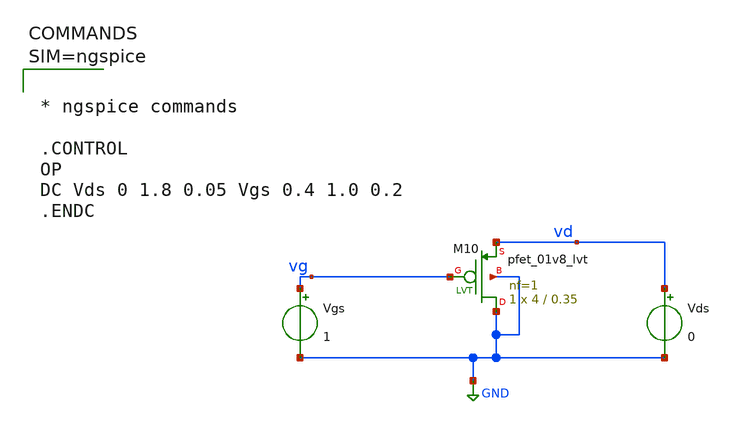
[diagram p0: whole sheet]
** sch_path: work/xschem/nmos_8.sch
**.subckt nmos_8
Vgs vg GND 1
Vds vd GND 0
XM10 GND vg vd GND sky130_fd_pr__pfet_01v8_lvt L=0.35 W=4 nf=1 ad='int((1 + 1)/2) * 4 / 1 * 0.29' as='int((1 + 2)/2) * 4 / 1 * 0.29'
+ pd='2*int((1 + 1)/2) * (4 / 1 + 0.29)' ps='2*int((1 + 2)/2) * (4 / 1 + 0.29)' nrd='0.29 / 4 ' nrs='0.29 / 4 '
+ sa=0 sb=0 sd=0 mult=1 m=1
**** begin user architecture code



* ngspice commands

.CONTROL
OP
DC Vds 0 1.8 0.05 Vgs 0.4 1.0 0.2
.ENDC




** opencircuitdesign pdks install
.lib $::SKYWATER_MODELS/sky130.lib.spice tt

**** end user architecture code
**.ends
.GLOBAL GND
.end
